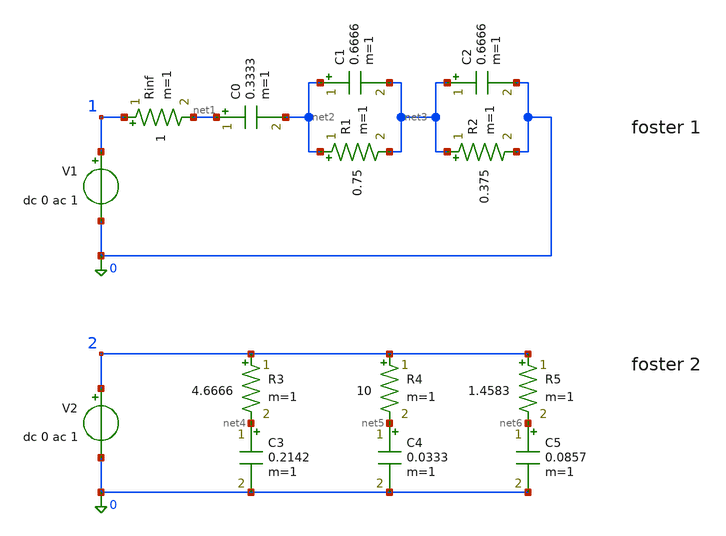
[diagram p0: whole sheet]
** sch_path: circuitos/exemplo06.sch
**.subckt exemplo06
C0 net1 net2 0.3333 m=1
V1 1 0 dc 0 ac 1
Rinf 1 net1 1 m=1
C1 net2 net3 0.6666 m=1
R1 net2 net3 0.75 m=1
C2 net3 0 0.6666 m=1
R2 net3 0 0.375 m=1
V2 2 0 dc 0 ac 1
C3 net4 0 0.2142 m=1
R3 2 net4 4.6666 m=1
C4 net5 0 0.0333 m=1
R4 2 net5 10 m=1
C5 net6 0 0.0857 m=1
R5 2 net6 1.4583 m=1
**** begin user architecture code

.control
ac dec 1001 1e-1 1e3

plot xlog real(-v(1)/v1#branch) imag(-v(1)/v1#branch)
plot xlog real(-v(2)/v2#branch) imag(-v(2)/v2#branch)

*plot xlog abs(-v(1)/v1#branch)
.endc

**** end user architecture code
**.ends
.end
